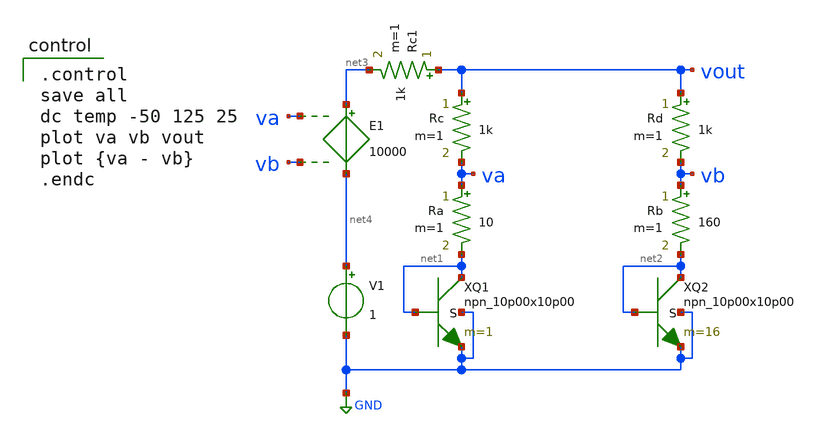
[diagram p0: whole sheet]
** sch_path: bgr/npn-diode-tc.sch
**.subckt npn-diode-tc
XQ1 net1 net1 GND GND npn_10p00x10p00 m=1
XQ2 net2 net2 GND GND npn_10p00x10p00 m=16
Rb vb net2 160 m=1
Ra va net1 10 m=1
Rc vout va 1k m=1
Rd vout vb 1k m=1
E1 net3 net4 va vb 10000
V1 net4 GND 1
Rc1 vout net3 1k m=1
**** begin user architecture code

.include $::180MCU_MODELS/design.ngspice
.lib $::180MCU_MODELS/sm141064.ngspice typical
.lib $::180MCU_MODELS/sm141064.ngspice res_typical
.lib $::180MCU_MODELS/sm141064.ngspice moscap_typical
.lib $::180MCU_MODELS/sm141064.ngspice bjt_typical
* .lib $::180MCU_MODELS/sm141064.ngspice res_statistical


.control
save all
dc temp -50 125 25
plot va vb vout
plot {va - vb}
.endc

**** end user architecture code
**.ends
.GLOBAL GND
.end
